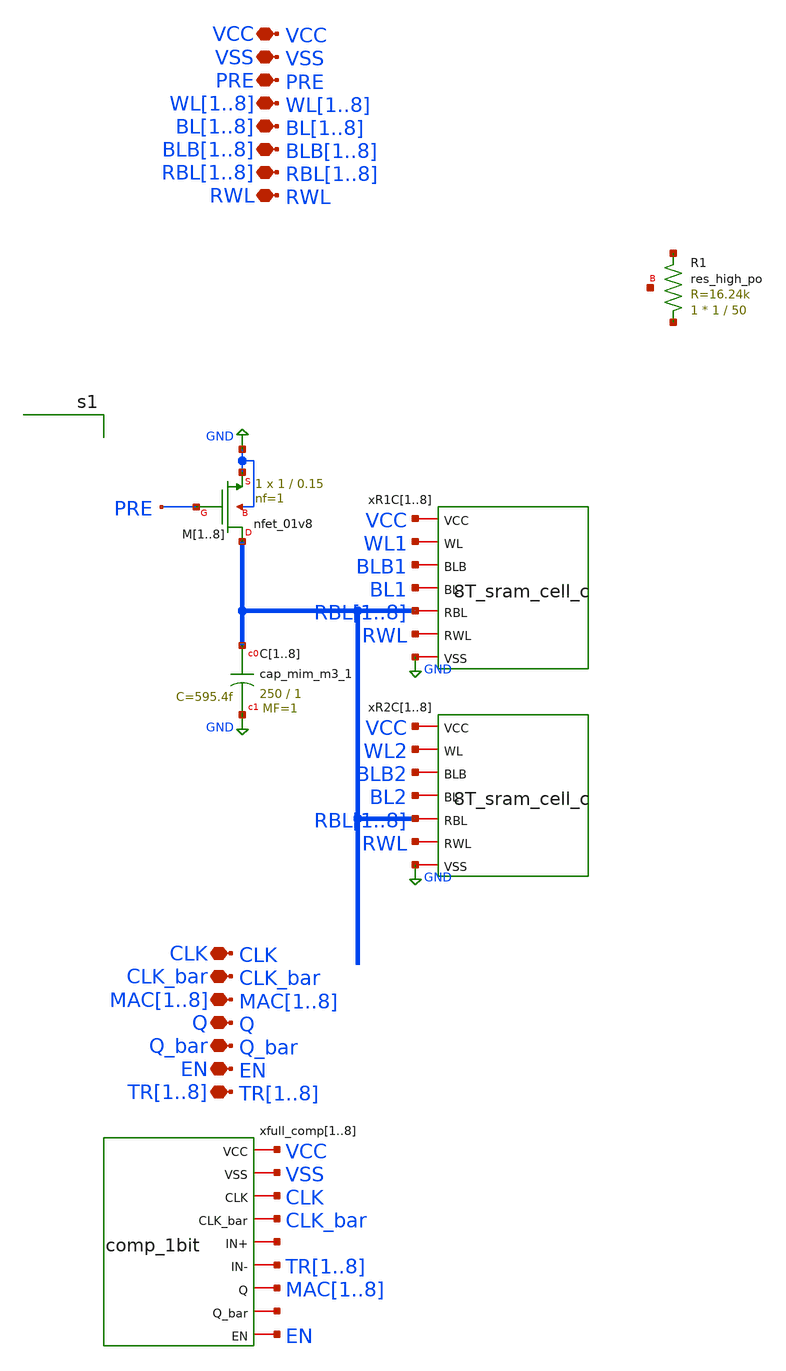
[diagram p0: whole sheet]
** sch_path: full_test_small.sch
**.subckt full_test_small VSS VCC PRE WL1,WL2,WL3,WL4,WL5,WL6,WL7,WL8
*+ BL1,BL2,BL3,BL4,BL5,BL6,BL7,BL8 BLB1,BLB2,BLB3,BLB4,BLB5,BLB6,BLB7,BLB8 RBL1,RBL2,RBL3,RBL4,RBL5,RBL6,RBL7,RBL8 RWL CLK CLK_bar Q
*+ Q_bar EN MAC1,MAC2,MAC3,MAC4,MAC5,MAC6,MAC7,MAC8 TR1,TR2,TR3,TR4,TR5,TR6,TR7,TR8
*.iopin VSS
*.iopin VCC
*.iopin PRE
*.iopin WL1,WL2,WL3,WL4,WL5,WL6,WL7,WL8
*.iopin BL1,BL2,BL3,BL4,BL5,BL6,BL7,BL8
*.iopin BLB1,BLB2,BLB3,BLB4,BLB5,BLB6,BLB7,BLB8
*.iopin RBL1,RBL2,RBL3,RBL4,RBL5,RBL6,RBL7,RBL8
*.iopin RWL
*.iopin CLK
*.iopin CLK_bar
*.iopin Q
*.iopin Q_bar
*.iopin EN
*.iopin MAC1,MAC2,MAC3,MAC4,MAC5,MAC6,MAC7,MAC8
*.iopin TR1,TR2,TR3,TR4,TR5,TR6,TR7,TR8
xR1C1 VCC WL1 BLB1 BL1 RBL1 RWL GND 8T_sram_cell_c
xR1C2 VCC WL1 BLB1 BL1 RBL2 RWL GND 8T_sram_cell_c
xR1C3 VCC WL1 BLB1 BL1 RBL3 RWL GND 8T_sram_cell_c
xR1C4 VCC WL1 BLB1 BL1 RBL4 RWL GND 8T_sram_cell_c
xR1C5 VCC WL1 BLB1 BL1 RBL5 RWL GND 8T_sram_cell_c
xR1C6 VCC WL1 BLB1 BL1 RBL6 RWL GND 8T_sram_cell_c
xR1C7 VCC WL1 BLB1 BL1 RBL7 RWL GND 8T_sram_cell_c
xR1C8 VCC WL1 BLB1 BL1 RBL8 RWL GND 8T_sram_cell_c
XC1 RBL1 GND sky130_fd_pr__cap_mim_m3_1 W=250 L=1 MF=1 m=1
XC2 RBL2 GND sky130_fd_pr__cap_mim_m3_1 W=250 L=1 MF=1 m=1
XC3 RBL3 GND sky130_fd_pr__cap_mim_m3_1 W=250 L=1 MF=1 m=1
XC4 RBL4 GND sky130_fd_pr__cap_mim_m3_1 W=250 L=1 MF=1 m=1
XC5 RBL5 GND sky130_fd_pr__cap_mim_m3_1 W=250 L=1 MF=1 m=1
XC6 RBL6 GND sky130_fd_pr__cap_mim_m3_1 W=250 L=1 MF=1 m=1
XC7 RBL7 GND sky130_fd_pr__cap_mim_m3_1 W=250 L=1 MF=1 m=1
XC8 RBL8 GND sky130_fd_pr__cap_mim_m3_1 W=250 L=1 MF=1 m=1
XR1 net1 net2 net3 sky130_fd_pr__res_high_po W=1 L=50 mult=1 m=1
xR2C1 VCC WL2 BLB2 BL2 RBL1 RWL GND 8T_sram_cell_c
xR2C2 VCC WL2 BLB2 BL2 RBL2 RWL GND 8T_sram_cell_c
xR2C3 VCC WL2 BLB2 BL2 RBL3 RWL GND 8T_sram_cell_c
xR2C4 VCC WL2 BLB2 BL2 RBL4 RWL GND 8T_sram_cell_c
xR2C5 VCC WL2 BLB2 BL2 RBL5 RWL GND 8T_sram_cell_c
xR2C6 VCC WL2 BLB2 BL2 RBL6 RWL GND 8T_sram_cell_c
xR2C7 VCC WL2 BLB2 BL2 RBL7 RWL GND 8T_sram_cell_c
xR2C8 VCC WL2 BLB2 BL2 RBL8 RWL GND 8T_sram_cell_c
XM1 RBL1 PRE GND GND sky130_fd_pr__nfet_01v8 L=0.15 W=1 nf=1 ad='int((1 + 1)/2) * 1 / 1 * 0.29' as='int((1 + 2)/2) * 1 / 1 * 0.29'
+ pd='2*int((1 + 1)/2) * (1 / 1 + 0.29)' ps='2*int((1 + 2)/2) * (1 / 1 + 0.29)' nrd='0.29 / 1 ' nrs='0.29 / 1 '
+ sa=0 sb=0 sd=0 mult=1 m=1
XM2 RBL2 PRE GND GND sky130_fd_pr__nfet_01v8 L=0.15 W=1 nf=1 ad='int((1 + 1)/2) * 1 / 1 * 0.29' as='int((1 + 2)/2) * 1 / 1 * 0.29'
+ pd='2*int((1 + 1)/2) * (1 / 1 + 0.29)' ps='2*int((1 + 2)/2) * (1 / 1 + 0.29)' nrd='0.29 / 1 ' nrs='0.29 / 1 '
+ sa=0 sb=0 sd=0 mult=1 m=1
XM3 RBL3 PRE GND GND sky130_fd_pr__nfet_01v8 L=0.15 W=1 nf=1 ad='int((1 + 1)/2) * 1 / 1 * 0.29' as='int((1 + 2)/2) * 1 / 1 * 0.29'
+ pd='2*int((1 + 1)/2) * (1 / 1 + 0.29)' ps='2*int((1 + 2)/2) * (1 / 1 + 0.29)' nrd='0.29 / 1 ' nrs='0.29 / 1 '
+ sa=0 sb=0 sd=0 mult=1 m=1
XM4 RBL4 PRE GND GND sky130_fd_pr__nfet_01v8 L=0.15 W=1 nf=1 ad='int((1 + 1)/2) * 1 / 1 * 0.29' as='int((1 + 2)/2) * 1 / 1 * 0.29'
+ pd='2*int((1 + 1)/2) * (1 / 1 + 0.29)' ps='2*int((1 + 2)/2) * (1 / 1 + 0.29)' nrd='0.29 / 1 ' nrs='0.29 / 1 '
+ sa=0 sb=0 sd=0 mult=1 m=1
XM5 RBL5 PRE GND GND sky130_fd_pr__nfet_01v8 L=0.15 W=1 nf=1 ad='int((1 + 1)/2) * 1 / 1 * 0.29' as='int((1 + 2)/2) * 1 / 1 * 0.29'
+ pd='2*int((1 + 1)/2) * (1 / 1 + 0.29)' ps='2*int((1 + 2)/2) * (1 / 1 + 0.29)' nrd='0.29 / 1 ' nrs='0.29 / 1 '
+ sa=0 sb=0 sd=0 mult=1 m=1
XM6 RBL6 PRE GND GND sky130_fd_pr__nfet_01v8 L=0.15 W=1 nf=1 ad='int((1 + 1)/2) * 1 / 1 * 0.29' as='int((1 + 2)/2) * 1 / 1 * 0.29'
+ pd='2*int((1 + 1)/2) * (1 / 1 + 0.29)' ps='2*int((1 + 2)/2) * (1 / 1 + 0.29)' nrd='0.29 / 1 ' nrs='0.29 / 1 '
+ sa=0 sb=0 sd=0 mult=1 m=1
XM7 RBL7 PRE GND GND sky130_fd_pr__nfet_01v8 L=0.15 W=1 nf=1 ad='int((1 + 1)/2) * 1 / 1 * 0.29' as='int((1 + 2)/2) * 1 / 1 * 0.29'
+ pd='2*int((1 + 1)/2) * (1 / 1 + 0.29)' ps='2*int((1 + 2)/2) * (1 / 1 + 0.29)' nrd='0.29 / 1 ' nrs='0.29 / 1 '
+ sa=0 sb=0 sd=0 mult=1 m=1
XM8 RBL8 PRE GND GND sky130_fd_pr__nfet_01v8 L=0.15 W=1 nf=1 ad='int((1 + 1)/2) * 1 / 1 * 0.29' as='int((1 + 2)/2) * 1 / 1 * 0.29'
+ pd='2*int((1 + 1)/2) * (1 / 1 + 0.29)' ps='2*int((1 + 2)/2) * (1 / 1 + 0.29)' nrd='0.29 / 1 ' nrs='0.29 / 1 '
+ sa=0 sb=0 sd=0 mult=1 m=1
xfull_comp1 VCC VSS CLK CLK_bar net4[7] TR1 MAC1 net5[7] EN comp_1bit
xfull_comp2 VCC VSS CLK CLK_bar net4[6] TR2 MAC2 net5[6] EN comp_1bit
xfull_comp3 VCC VSS CLK CLK_bar net4[5] TR3 MAC3 net5[5] EN comp_1bit
xfull_comp4 VCC VSS CLK CLK_bar net4[4] TR4 MAC4 net5[4] EN comp_1bit
xfull_comp5 VCC VSS CLK CLK_bar net4[3] TR5 MAC5 net5[3] EN comp_1bit
xfull_comp6 VCC VSS CLK CLK_bar net4[2] TR6 MAC6 net5[2] EN comp_1bit
xfull_comp7 VCC VSS CLK CLK_bar net4[1] TR7 MAC7 net5[1] EN comp_1bit
xfull_comp8 VCC VSS CLK CLK_bar net4[0] TR8 MAC8 net5[0] EN comp_1bit
**** begin user architecture code







.param VCC=1.8 VSS=0
V_VCC VCC 0 DC 1.8
V_VSS VSS 0 DC 0



** opencircuitdesign pdks install
.lib $::SKYWATER_MODELS/sky130.lib.spice tt

**** end user architecture code
**.ends
.GLOBAL GND
.end
